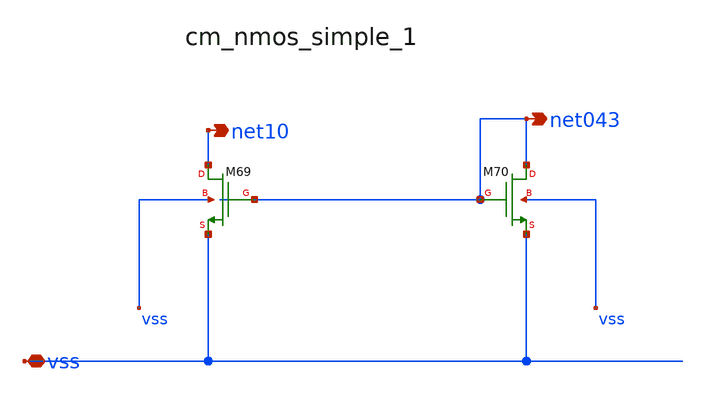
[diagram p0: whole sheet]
** sch_path: analog-db/raw/amp_012_peng_tcfc/hier/blocks/cm_nmos_simple_1.sch
**.subckt cm_nmos_simple_1 vss net10 net043
*.iopin vss
*.opin net10
*.opin net043
XM69 net10 net043 vss vss sg13_lv_nmos w=x_dut_xm69_w l=x_dut_xm69_l ng=1 m=x_dut_xm69_m
XM70 net043 net043 vss vss sg13_lv_nmos w=x_dut_xm70_w l=x_dut_xm70_l ng=1 m=x_dut_xm70_m
**.ends
.end
